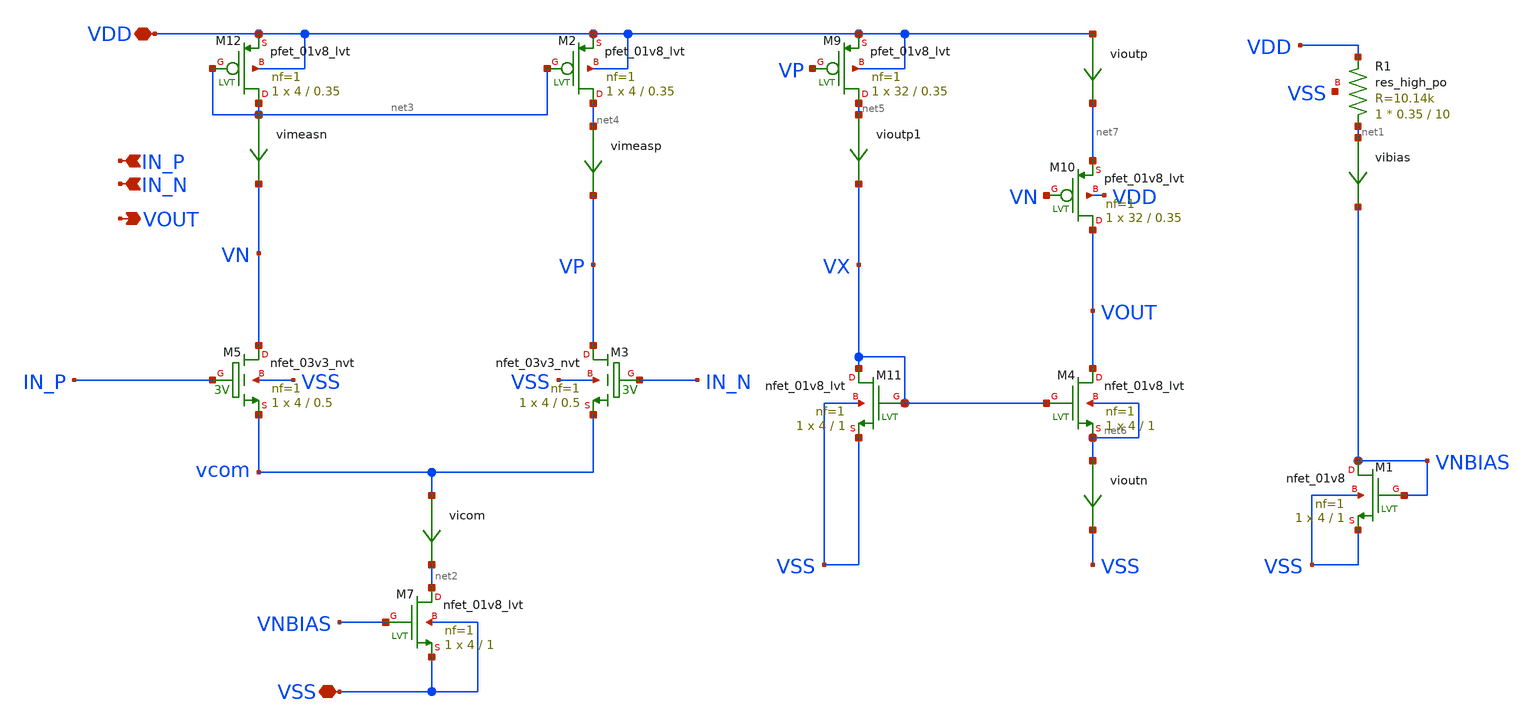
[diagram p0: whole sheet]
** sch_path: xschem/opamp2.sch
**.subckt opamp2 VDD VSS IN_N VOUT IN_P
*.iopin VDD
*.iopin VSS
*.ipin IN_N
*.opin VOUT
*.ipin IN_P
XR1 net1 VDD VSS sky130_fd_pr__res_high_po W=0.35 L=10 mult=1 m=1
vibias net1 VNBIAS 0
.save i(vibias)
XM1 VNBIAS VNBIAS VSS VSS sky130_fd_pr__nfet_01v8 L=1 W=4 nf=1 ad='int((nf+1)/2) * W/nf * 0.29' as='int((nf+2)/2) * W/nf * 0.29'
+ pd='2*int((nf+1)/2) * (W/nf + 0.29)' ps='2*int((nf+2)/2) * (W/nf + 0.29)' nrd='0.29 / W' nrs='0.29 / W'
+ sa=0 sb=0 sd=0 mult=1 m=1
vimeasn net3 VN 0
.save i(vimeasn)
vimeasp net4 VP 0
.save i(vimeasp)
vicom vcom net2 0
.save i(vicom)
XM7 net2 VNBIAS VSS VSS sky130_fd_pr__nfet_01v8_lvt L=1 W=4 nf=1 ad='int((nf+1)/2) * W/nf * 0.29' as='int((nf+2)/2) * W/nf * 0.29'
+ pd='2*int((nf+1)/2) * (W/nf + 0.29)' ps='2*int((nf+2)/2) * (W/nf + 0.29)' nrd='0.29 / W' nrs='0.29 / W'
+ sa=0 sb=0 sd=0 mult=1 m=1
vioutp1 net5 VX 0
.save i(vioutp1)
XM4 VOUT VX net6 net6 sky130_fd_pr__nfet_01v8_lvt L=1 W=4 nf=1 ad='int((nf+1)/2) * W/nf * 0.29' as='int((nf+2)/2) * W/nf * 0.29'
+ pd='2*int((nf+1)/2) * (W/nf + 0.29)' ps='2*int((nf+2)/2) * (W/nf + 0.29)' nrd='0.29 / W' nrs='0.29 / W'
+ sa=0 sb=0 sd=0 mult=1 m=1
XM11 VX VX VSS VSS sky130_fd_pr__nfet_01v8_lvt L=1 W=4 nf=1 ad='int((nf+1)/2) * W/nf * 0.29' as='int((nf+2)/2) * W/nf * 0.29'
+ pd='2*int((nf+1)/2) * (W/nf + 0.29)' ps='2*int((nf+2)/2) * (W/nf + 0.29)' nrd='0.29 / W' nrs='0.29 / W'
+ sa=0 sb=0 sd=0 mult=1 m=1
vioutp VDD net7 0
.save i(vioutp)
vioutn net6 VSS 0
.save i(vioutn)
XM12 net3 net3 VDD VDD sky130_fd_pr__pfet_01v8_lvt L=0.35 W=4 nf=1 ad='int((nf+1)/2) * W/nf * 0.29' as='int((nf+2)/2) * W/nf * 0.29'
+ pd='2*int((nf+1)/2) * (W/nf + 0.29)' ps='2*int((nf+2)/2) * (W/nf + 0.29)' nrd='0.29 / W' nrs='0.29 / W'
+ sa=0 sb=0 sd=0 mult=1 m=1
XM2 net4 net3 VDD VDD sky130_fd_pr__pfet_01v8_lvt L=0.35 W=4 nf=1 ad='int((nf+1)/2) * W/nf * 0.29' as='int((nf+2)/2) * W/nf * 0.29'
+ pd='2*int((nf+1)/2) * (W/nf + 0.29)' ps='2*int((nf+2)/2) * (W/nf + 0.29)' nrd='0.29 / W' nrs='0.29 / W'
+ sa=0 sb=0 sd=0 mult=1 m=1
XM9 net5 VP VDD VDD sky130_fd_pr__pfet_01v8_lvt L=0.35 W=32 nf=1 ad='int((nf+1)/2) * W/nf * 0.29' as='int((nf+2)/2) * W/nf * 0.29'
+ pd='2*int((nf+1)/2) * (W/nf + 0.29)' ps='2*int((nf+2)/2) * (W/nf + 0.29)' nrd='0.29 / W' nrs='0.29 / W'
+ sa=0 sb=0 sd=0 mult=1 m=1
XM10 VOUT VN net7 VDD sky130_fd_pr__pfet_01v8_lvt L=0.35 W=32 nf=1 ad='int((nf+1)/2) * W/nf * 0.29' as='int((nf+2)/2) * W/nf * 0.29'
+ pd='2*int((nf+1)/2) * (W/nf + 0.29)' ps='2*int((nf+2)/2) * (W/nf + 0.29)' nrd='0.29 / W' nrs='0.29 / W'
+ sa=0 sb=0 sd=0 mult=1 m=1
XM3 VP IN_N vcom VSS sky130_fd_pr__nfet_03v3_nvt L=0.5 W=4 nf=1 ad='int((nf+1)/2) * W/nf * 0.29' as='int((nf+2)/2) * W/nf * 0.29'
+ pd='2*int((nf+1)/2) * (W/nf + 0.29)' ps='2*int((nf+2)/2) * (W/nf + 0.29)' nrd='0.29 / W' nrs='0.29 / W'
+ sa=0 sb=0 sd=0 mult=1 m=1
XM5 VN IN_P vcom VSS sky130_fd_pr__nfet_03v3_nvt L=0.5 W=4 nf=1 ad='int((nf+1)/2) * W/nf * 0.29' as='int((nf+2)/2) * W/nf * 0.29'
+ pd='2*int((nf+1)/2) * (W/nf + 0.29)' ps='2*int((nf+2)/2) * (W/nf + 0.29)' nrd='0.29 / W' nrs='0.29 / W'
+ sa=0 sb=0 sd=0 mult=1 m=1
**.ends
.end
